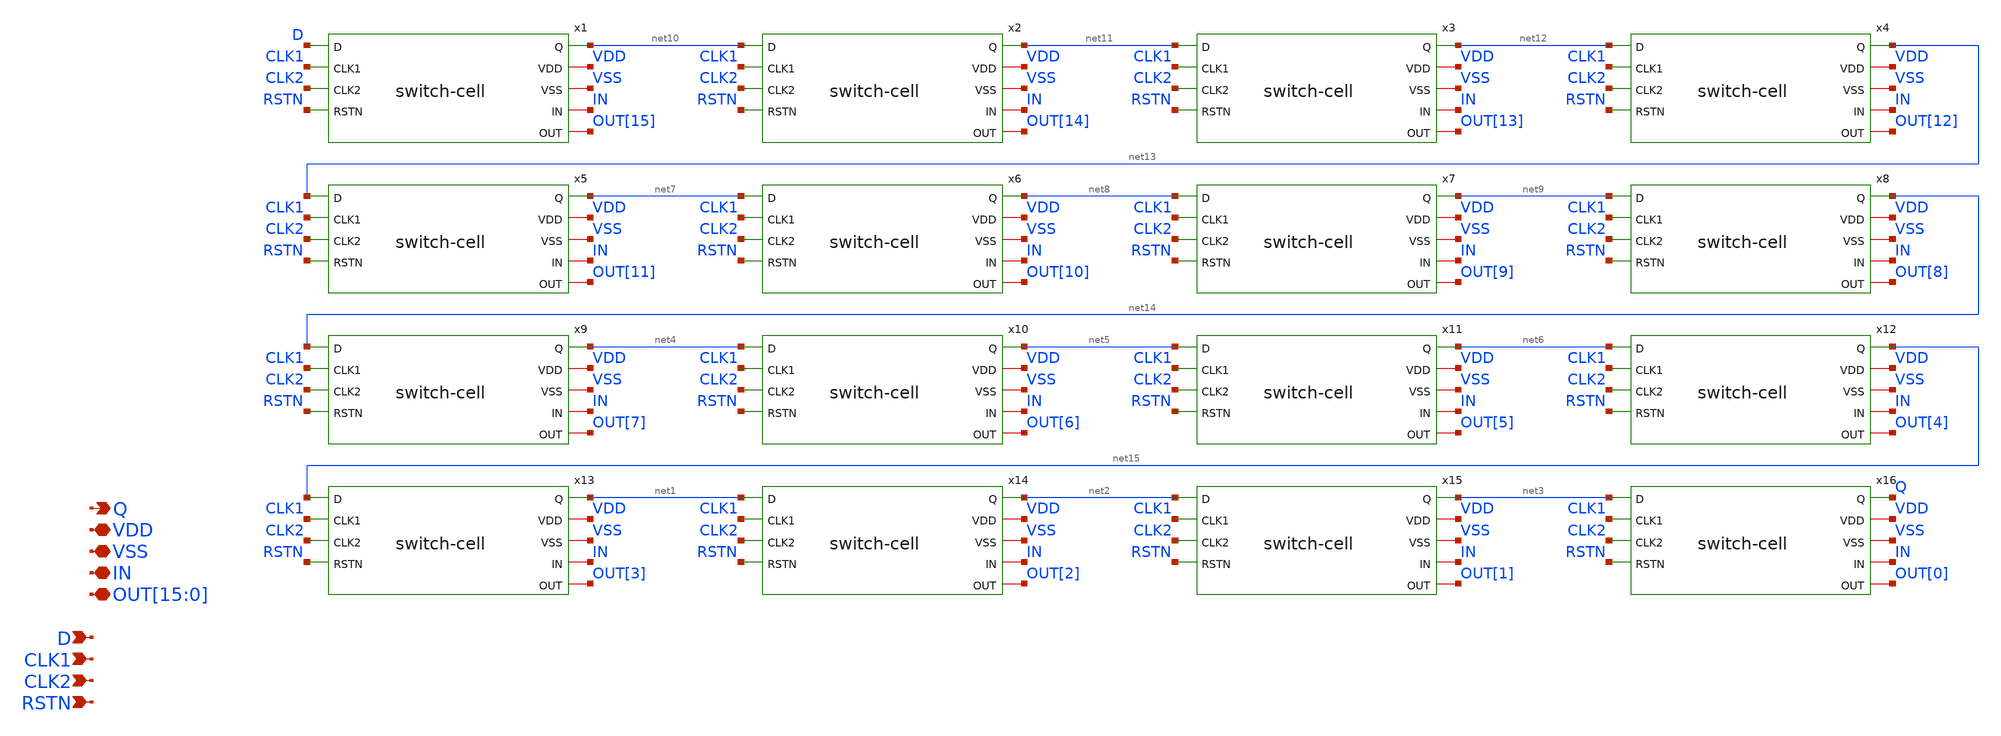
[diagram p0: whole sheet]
** sch_path: designs/libs/core_switch-matrix/switch-matrix-16x1/switch-matrix-16x1.sch
**.subckt switch-matrix-16x1 VDD VSS IN
*+ OUT[15],OUT[14],OUT[13],OUT[12],OUT[11],OUT[10],OUT[9],OUT[8],OUT[7],OUT[6],OUT[5],OUT[4],OUT[3],OUT[2],OUT[1],OUT[0] D RSTN Q CLK1 CLK2
*.iopin VDD
*.iopin VSS
*.iopin IN
*.iopin
*+ OUT[15],OUT[14],OUT[13],OUT[12],OUT[11],OUT[10],OUT[9],OUT[8],OUT[7],OUT[6],OUT[5],OUT[4],OUT[3],OUT[2],OUT[1],OUT[0]
*.ipin D
*.ipin RSTN
*.opin Q
*.ipin CLK1
*.ipin CLK2
x1 net10 VDD VSS D CLK1 CLK2 RSTN IN OUT[15] switch-cell
x2 net11 VDD VSS net10 CLK1 CLK2 RSTN IN OUT[14] switch-cell
x3 net12 VDD VSS net11 CLK1 CLK2 RSTN IN OUT[13] switch-cell
x4 net13 VDD VSS net12 CLK1 CLK2 RSTN IN OUT[12] switch-cell
x5 net7 VDD VSS net13 CLK1 CLK2 RSTN IN OUT[11] switch-cell
x6 net8 VDD VSS net7 CLK1 CLK2 RSTN IN OUT[10] switch-cell
x7 net9 VDD VSS net8 CLK1 CLK2 RSTN IN OUT[9] switch-cell
x8 net14 VDD VSS net9 CLK1 CLK2 RSTN IN OUT[8] switch-cell
x9 net4 VDD VSS net14 CLK1 CLK2 RSTN IN OUT[7] switch-cell
x10 net5 VDD VSS net4 CLK1 CLK2 RSTN IN OUT[6] switch-cell
x11 net6 VDD VSS net5 CLK1 CLK2 RSTN IN OUT[5] switch-cell
x12 net15 VDD VSS net6 CLK1 CLK2 RSTN IN OUT[4] switch-cell
x13 net1 VDD VSS net15 CLK1 CLK2 RSTN IN OUT[3] switch-cell
x14 net2 VDD VSS net1 CLK1 CLK2 RSTN IN OUT[2] switch-cell
x15 net3 VDD VSS net2 CLK1 CLK2 RSTN IN OUT[1] switch-cell
x16 Q VDD VSS net3 CLK1 CLK2 RSTN IN OUT[0] switch-cell
**.ends
.end
